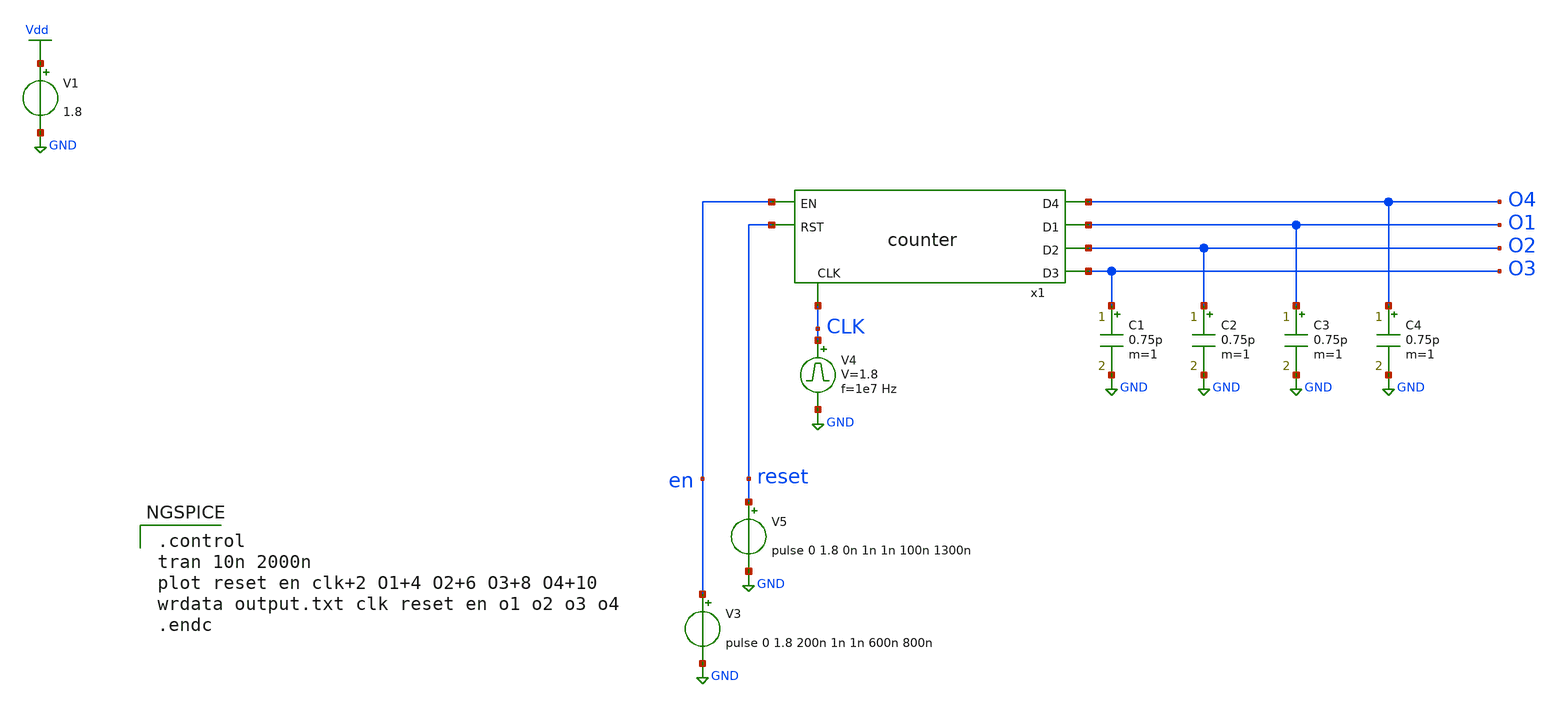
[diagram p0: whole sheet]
** sch_path: Circuiti/counter/test.sch
**.subckt test
V1 Vdd GND 1.8
C1 O3 GND 0.75p m=1
V3 en GND pulse 0 1.8 200n 1n 1n 600n 800n
C2 O2 GND 0.75p m=1
V5 reset GND pulse 0 1.8 0n 1n 1n 100n 1300n
x1 O4 O1 O2 O3 en CLK reset counter
C3 O1 GND 0.75p m=1
C4 O4 GND 0.75p m=1
V4 CLK GND pulse 0 1.8 '0.495/ 1e7 ' '0.01/1e7 ' '0.01/1e7 ' '0.49/1e7 ' '1/1e7 '
**** begin user architecture code


.lib /home/matteo/xschem_downloads/skywater-pdk/libraries/sky130_fd_pr_ngspice/latest/models/sky130.lib.spice tt

*.include /home/matteo/xschem_downloads/skywater-pdk/libraries/sky130_fd_pr_ngspice/latest/cells/nfet_01v8/sky130_fd_pr__nfet_01v8__tt.corner.spice

.param mc_mm_switch=0
.param mc_pr_switch=1



.control
tran 10n 2000n
plot reset en clk+2 O1+4 O2+6 O3+8 O4+10
wrdata output.txt clk reset en o1 o2 o3 o4
.endc



.ic v(r1)=0
.ic v(r2)=0
.ic v(r3)=0
.ic v(r4)=0

**** end user architecture code
**.ends
.GLOBAL GND
.GLOBAL Vdd
.end
